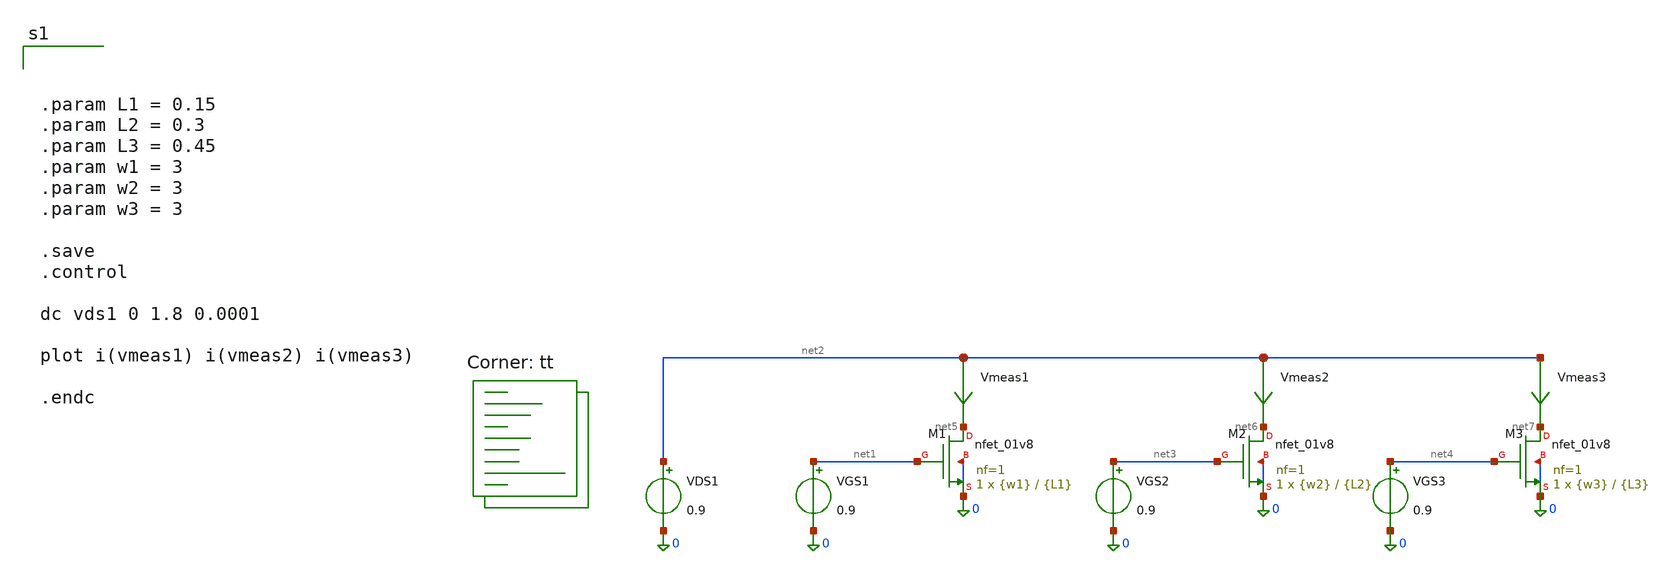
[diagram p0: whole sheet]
** sch_path: Training-3/clm.sch
**.subckt clm
Vmeas1 net2 net5 0
.save i(vmeas1)
VGS1 net1 0 0.9
XM1 net5 net1 0 0 sky130_fd_pr__nfet_01v8 L={L1} W={w1} nf=1 ad='int((nf+1)/2) * W/nf * 0.29' as='int((nf+2)/2) * W/nf * 0.29'
+ pd='2*int((nf+1)/2) * (W/nf + 0.29)' ps='2*int((nf+2)/2) * (W/nf + 0.29)' nrd='0.29 / W' nrs='0.29 / W'
+ sa=0 sb=0 sd=0 mult=1 m=1
VDS1 net2 0 0.9
Vmeas2 net2 net6 0
.save i(vmeas2)
VGS2 net3 0 0.9
XM2 net6 net3 0 0 sky130_fd_pr__nfet_01v8 L={L2} W={w2} nf=1 ad='int((nf+1)/2) * W/nf * 0.29' as='int((nf+2)/2) * W/nf * 0.29'
+ pd='2*int((nf+1)/2) * (W/nf + 0.29)' ps='2*int((nf+2)/2) * (W/nf + 0.29)' nrd='0.29 / W' nrs='0.29 / W'
+ sa=0 sb=0 sd=0 mult=1 m=1
Vmeas3 net2 net7 0
.save i(vmeas3)
VGS3 net4 0 0.9
XM3 net7 net4 0 0 sky130_fd_pr__nfet_01v8 L={L3} W={w3} nf=1 ad='int((nf+1)/2) * W/nf * 0.29' as='int((nf+2)/2) * W/nf * 0.29'
+ pd='2*int((nf+1)/2) * (W/nf + 0.29)' ps='2*int((nf+2)/2) * (W/nf + 0.29)' nrd='0.29 / W' nrs='0.29 / W'
+ sa=0 sb=0 sd=0 mult=1 m=1
**** begin user architecture code



.param L1 = 0.15
.param L2 = 0.3
.param L3 = 0.45
.param w1 = 3
.param w2 = 3
.param w3 = 3

.save
.control

dc vds1 0 1.8 0.0001

plot i(vmeas1) i(vmeas2) i(vmeas3)

.endc




.lib $::SKYWATER_MODELS/sky130.lib.spice tt
**** end user architecture code
**.ends
.end
